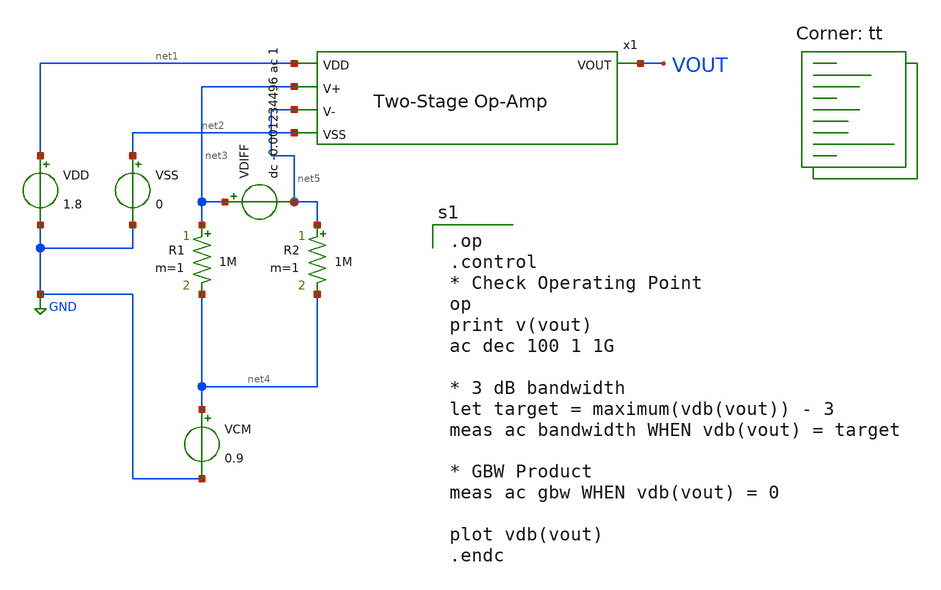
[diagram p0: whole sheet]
** sch_path: analog/schematics/tb_ac_analysis.sch
**.subckt tb_ac_analysis
VDD net1 GND 1.8
VSS net2 GND 0
VCM net4 GND 0.9
VDIFF net3 net5 dc -0.001234496 ac 1
R1 net3 net4 1M m=1
R2 net5 net4 1M m=1
x1 net1 net3 net5 VOUT net2 bootcamp_opamp
**** begin user architecture code

.op
.control
* Check Operating Point
op
print v(vout)
ac dec 100 1 1G

* 3 dB bandwidth
let target = maximum(vdb(vout)) - 3
meas ac bandwidth WHEN vdb(vout) = target

* GBW Product
meas ac gbw WHEN vdb(vout) = 0

plot vdb(vout)
.endc

.lib $::SKYWATER_MODELS/sky130.lib.spice tt
**** end user architecture code
**.ends

* expanding   symbol:  bootcamp_opamp.sym # of pins=5
** sym_path: analog/schematics/bootcamp_opamp.sym
** sch_path: analog/schematics/bootcamp_opamp.sch
.subckt bootcamp_opamp VDD V+ V- VOUT VSS
*.ipin V+
*.ipin V-
*.opin VOUT
*.ipin VDD
*.ipin VSS
XM1 net1 V+ net3 VSS sky130_fd_pr__nfet_01v8 L=1 W=4 nf=1 ad='int((nf+1)/2) * W/nf * 0.29' as='int((nf+2)/2) * W/nf * 0.29'
+ pd='2*int((nf+1)/2) * (W/nf + 0.29)' ps='2*int((nf+2)/2) * (W/nf + 0.29)' nrd='0.29 / W' nrs='0.29 / W'
+ sa=0 sb=0 sd=0 mult=1 m=1
XM2 net2 V- net3 VSS sky130_fd_pr__nfet_01v8 L=1 W=4 nf=1 ad='int((nf+1)/2) * W/nf * 0.29' as='int((nf+2)/2) * W/nf * 0.29'
+ pd='2*int((nf+1)/2) * (W/nf + 0.29)' ps='2*int((nf+2)/2) * (W/nf + 0.29)' nrd='0.29 / W' nrs='0.29 / W'
+ sa=0 sb=0 sd=0 mult=1 m=1
XM3 net1 net1 VDD VDD sky130_fd_pr__pfet_01v8 L=1 W=4 nf=1 ad='int((nf+1)/2) * W/nf * 0.29' as='int((nf+2)/2) * W/nf * 0.29'
+ pd='2*int((nf+1)/2) * (W/nf + 0.29)' ps='2*int((nf+2)/2) * (W/nf + 0.29)' nrd='0.29 / W' nrs='0.29 / W'
+ sa=0 sb=0 sd=0 mult=1 m=1
XM4 net2 net1 VDD VDD sky130_fd_pr__pfet_01v8 L=1 W=4 nf=1 ad='int((nf+1)/2) * W/nf * 0.29' as='int((nf+2)/2) * W/nf * 0.29'
+ pd='2*int((nf+1)/2) * (W/nf + 0.29)' ps='2*int((nf+2)/2) * (W/nf + 0.29)' nrd='0.29 / W' nrs='0.29 / W'
+ sa=0 sb=0 sd=0 mult=1 m=1
XM5 net3 net4 VSS VSS sky130_fd_pr__nfet_01v8 L=2 W=4 nf=1 ad='int((nf+1)/2) * W/nf * 0.29' as='int((nf+2)/2) * W/nf * 0.29'
+ pd='2*int((nf+1)/2) * (W/nf + 0.29)' ps='2*int((nf+2)/2) * (W/nf + 0.29)' nrd='0.29 / W' nrs='0.29 / W'
+ sa=0 sb=0 sd=0 mult=1 m=1
XM6 net4 net4 VSS VSS sky130_fd_pr__nfet_01v8 L=2 W=4 nf=1 ad='int((nf+1)/2) * W/nf * 0.29' as='int((nf+2)/2) * W/nf * 0.29'
+ pd='2*int((nf+1)/2) * (W/nf + 0.29)' ps='2*int((nf+2)/2) * (W/nf + 0.29)' nrd='0.29 / W' nrs='0.29 / W'
+ sa=0 sb=0 sd=0 mult=1 m=1
XM8 VOUT net4 VSS VSS sky130_fd_pr__nfet_01v8 L=0.5 W=2 nf=1 ad='int((nf+1)/2) * W/nf * 0.29' as='int((nf+2)/2) * W/nf * 0.29'
+ pd='2*int((nf+1)/2) * (W/nf + 0.29)' ps='2*int((nf+2)/2) * (W/nf + 0.29)' nrd='0.29 / W' nrs='0.29 / W'
+ sa=0 sb=0 sd=0 mult=1 m=1
XC1 net2 VOUT sky130_fd_pr__cap_mim_m3_1 W=22 L=22 MF=1 m=1
R1 VDD net4 12k m=1
XM7 VOUT net2 VDD VDD sky130_fd_pr__pfet_01v8 L=0.5 W=8 nf=1 ad='int((nf+1)/2) * W/nf * 0.29' as='int((nf+2)/2) * W/nf * 0.29'
+ pd='2*int((nf+1)/2) * (W/nf + 0.29)' ps='2*int((nf+2)/2) * (W/nf + 0.29)' nrd='0.29 / W' nrs='0.29 / W'
+ sa=0 sb=0 sd=0 mult=1 m=1
.ends

.GLOBAL GND
.end
